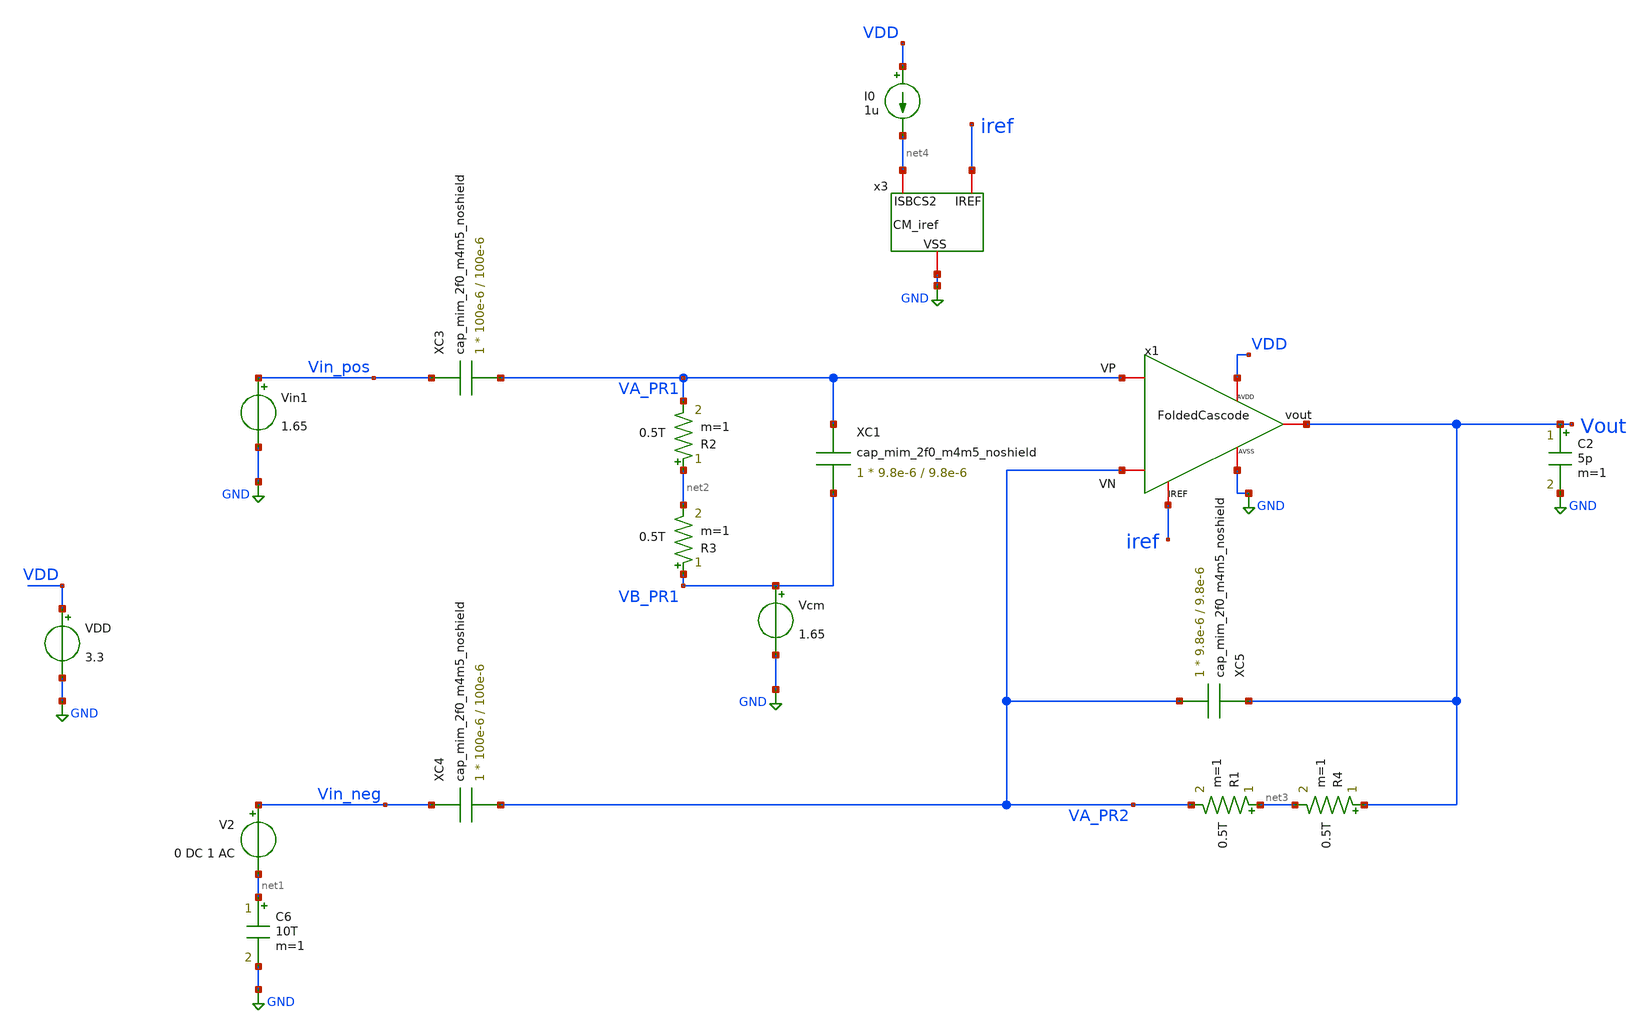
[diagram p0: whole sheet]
** sch_path: TIA_Filter/TB_filter_noPR_ac.sch
**.subckt TB_filter_noPR_ac
VDD VDD GND 3.3
C2 Vout GND 5p m=1
x1 VA_PR1 VA_PR2 Vout iref VDD GND FoldedCascode
I0 VDD net4 1u
Vcm VB_PR1 GND 1.65
Vin1 Vin_pos GND 1.65
V2 Vin_neg net1 0 DC 1 AC
C6 net1 GND 10T m=1
R1 net3 VA_PR2 0.5T m=1
R2 net2 VA_PR1 0.5T m=1
R3 VB_PR1 net2 0.5T m=1
R4 Vout net3 0.5T m=1
XC1 VA_PR1 VB_PR1 cap_mim_2f0_m4m5_noshield c_width=9.8e-6 c_length=9.8e-6 m=1
XC5 Vout VA_PR2 cap_mim_2f0_m4m5_noshield c_width=9.8e-6 c_length=9.8e-6 m=1
XC3 Vin_pos VA_PR1 cap_mim_2f0_m4m5_noshield c_width=100e-6 c_length=100e-6 m=1
XC4 Vin_neg VA_PR2 cap_mim_2f0_m4m5_noshield c_width=100e-6 c_length=100e-6 m=1
x3 net4 iref GND CM_iref
**** begin user architecture code

.include $::180MCU_MODELS/design.ngspice
.lib $::180MCU_MODELS/sm141064.ngspice typical
.lib $::180MCU_MODELS/sm141064.ngspice cap_mim
.lib $::180MCU_MODELS/sm141064.ngspice res_typical
.lib $::180MCU_MODELS/sm141064.ngspice moscap_typical
.lib $::180MCU_MODELS/sm141064.ngspice mimcap_typical



.option gmin=1e-16

.param ibias = 1p
.param it_amp = 2p

.control
save all

*tran 10u 10m
*remzerovec
*write TB_TIA_ac.raw
*set appendwrite

op
remzerovec
write TB_filter_noPR_ac.raw
set appendwrite

ac dec 10 1m 1e8
remzerovec
write TB_filter_noPR_ac.raw


.endc


**** end user architecture code
**.ends
.GLOBAL GND
.end
